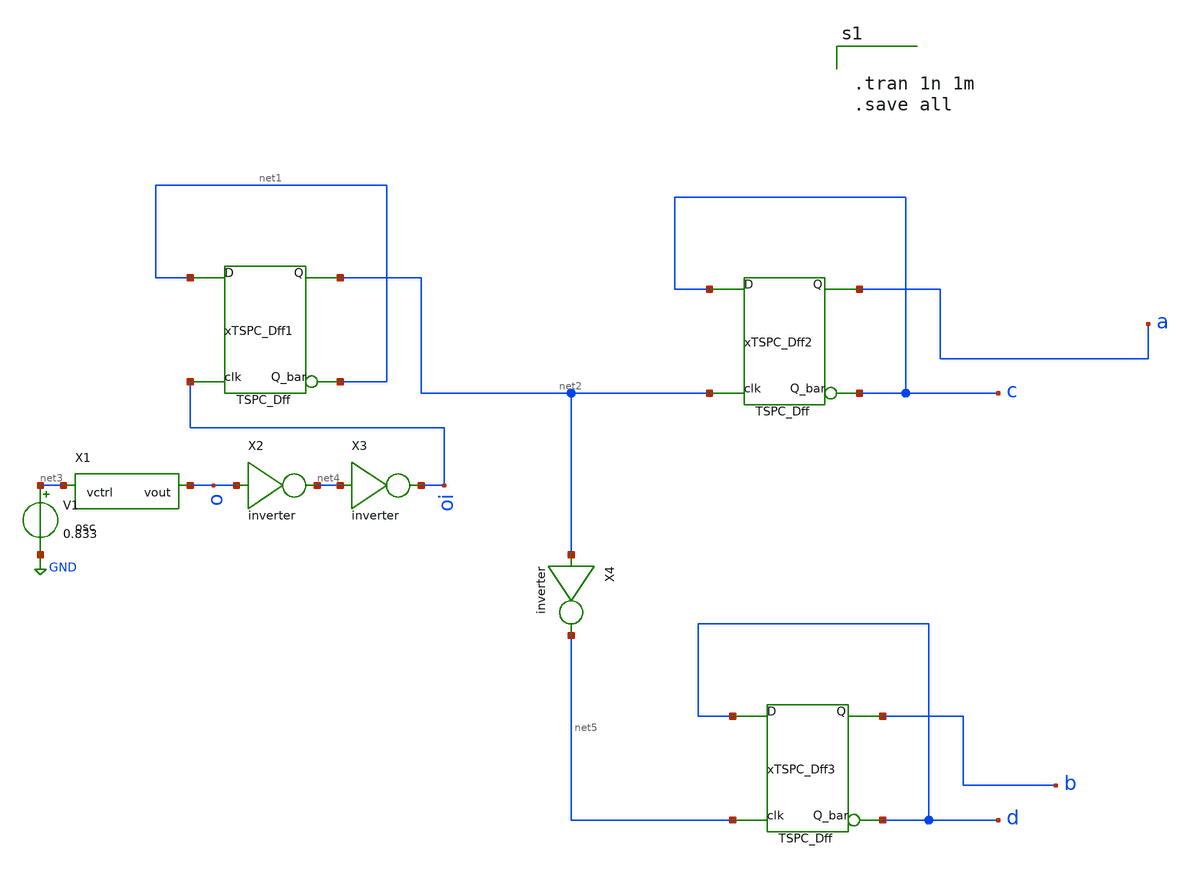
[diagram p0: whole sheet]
** sch_path: bfour.sch
**.subckt bfour
xTSPC_Dff1 oi net1 net1 net2 TSPC_Dff
X1 net3 o osc
V1 net3 GND 0.833
X2 o net4 inverter
X3 net4 oi inverter
xTSPC_Dff2 net2 c c a TSPC_Dff
xTSPC_Dff3 net5 d d b TSPC_Dff
X4 net2 net5 inverter
**** begin user architecture code


.tran 1n 1m
.save all


*.lib ~/open_pdks/sky130/sky130A/libs.tech/ngspice/sky130.lib.spice tt
.param mc_mm_switch=0
.param mc_pr_switch=0

.include ~/open_pdks/sky130/sky130A/libs.tech/ngspice/corners/tt/nonfet.spice


*model
.include ~/open_pdks/sky130/sky130A/libs.tech/ngspice/all.spice

*mosfet
.include ~/open_pdks/sky130/sky130A/libs.ref/sky130_fd_pr/spice/sky130_fd_pr__pfet_01v8__tt.corner.spice
.inclued ~/open_pdks/sky130/sky130A/libs.ref/sky130_fd_pr/spice/sky130_fd_pr__nfet_01v8__tt.corner.spice

*mismatch parameters
.include ~/open_pdks/sky130/sky130A/libs.ref/sky130_fd_pr/spice/sky130_fd_pr__pfet_01v8__mismatch.corner.spice
.include ~/open_pdks/sky130/sky130A/libs.ref/sky130_fd_pr/spice/sky130_fd_pr__nfet_01v8__mismatch.corner.spice

**** end user architecture code
**.ends

* expanding   symbol:  /home/cegrahul/Downloads/TSPC_Dff.sym # of pins=4
** sym_path: TSPC_Dff.sym
** sch_path: TSPC_Dff.sch
.subckt TSPC_Dff CLK D QB Q
*.ipin D
*.ipin CLK
*.opin Q
*.opin QB
V1 VDD GND 1.8
XM3 voutfirst D GND GND sky130_fd_pr__nfet_01v8 L=0.15 W=0.36 nf=1 ad='int((nf+1)/2) * W/nf * 0.29' as='int((nf+2)/2) * W/nf * 0.29'
+ pd='2*int((nf+1)/2) * (W/nf + 0.29)' ps='2*int((nf+2)/2) * (W/nf + 0.29)' nrd='0.29 / W' nrs='0.29 / W'
+ sa=0 sb=0 sd=0 mult=1 m=1
XM4 net1 D VDD VDD sky130_fd_pr__pfet_01v8 L=0.15 W=1.68 nf=1 ad='int((nf+1)/2) * W/nf * 0.29' as='int((nf+2)/2) * W/nf * 0.29'
+ pd='2*int((nf+1)/2) * (W/nf + 0.29)' ps='2*int((nf+2)/2) * (W/nf + 0.29)' nrd='0.29 / W' nrs='0.29 / W'
+ sa=0 sb=0 sd=0 mult=1 m=1
XM5 voutfirst CLK net1 VDD sky130_fd_pr__pfet_01v8 L=0.15 W=1.68 nf=1 ad='int((nf+1)/2) * W/nf * 0.29'
+ as='int((nf+2)/2) * W/nf * 0.29' pd='2*int((nf+1)/2) * (W/nf + 0.29)' ps='2*int((nf+2)/2) * (W/nf + 0.29)'
+ nrd='0.29 / W' nrs='0.29 / W' sa=0 sb=0 sd=0 mult=1 m=1
XM1 net3 CLK GND GND sky130_fd_pr__nfet_01v8 L=0.15 W=0.36 nf=1 ad='int((nf+1)/2) * W/nf * 0.29' as='int((nf+2)/2) * W/nf * 0.29'
+ pd='2*int((nf+1)/2) * (W/nf + 0.29)' ps='2*int((nf+2)/2) * (W/nf + 0.29)' nrd='0.29 / W' nrs='0.29 / W'
+ sa=0 sb=0 sd=0 mult=1 m=1
XM2 net2 CLK VDD VDD sky130_fd_pr__pfet_01v8 L=0.15 W=1.68 nf=1 ad='int((nf+1)/2) * W/nf * 0.29' as='int((nf+2)/2) * W/nf * 0.29'
+ pd='2*int((nf+1)/2) * (W/nf + 0.29)' ps='2*int((nf+2)/2) * (W/nf + 0.29)' nrd='0.29 / W' nrs='0.29 / W'
+ sa=0 sb=0 sd=0 mult=1 m=1
XM6 net2 voutfirst net3 GND sky130_fd_pr__nfet_01v8 L=0.15 W=0.36 nf=1 ad='int((nf+1)/2) * W/nf * 0.29'
+ as='int((nf+2)/2) * W/nf * 0.29' pd='2*int((nf+1)/2) * (W/nf + 0.29)' ps='2*int((nf+2)/2) * (W/nf + 0.29)'
+ nrd='0.29 / W' nrs='0.29 / W' sa=0 sb=0 sd=0 mult=1 m=1
XM7 net4 net2 GND GND sky130_fd_pr__nfet_01v8 L=2 W=0.42 nf=1 ad='int((nf+1)/2) * W/nf * 0.29' as='int((nf+2)/2) * W/nf * 0.29'
+ pd='2*int((nf+1)/2) * (W/nf + 0.29)' ps='2*int((nf+2)/2) * (W/nf + 0.29)' nrd='0.29 / W' nrs='0.29 / W'
+ sa=0 sb=0 sd=0 mult=1 m=1
XM8 voutthird net2 VDD VDD sky130_fd_pr__pfet_01v8 L=0.15 W=1.68 nf=1 ad='int((nf+1)/2) * W/nf * 0.29'
+ as='int((nf+2)/2) * W/nf * 0.29' pd='2*int((nf+1)/2) * (W/nf + 0.29)' ps='2*int((nf+2)/2) * (W/nf + 0.29)'
+ nrd='0.29 / W' nrs='0.29 / W' sa=0 sb=0 sd=0 mult=1 m=1
XM9 voutthird CLK net4 GND sky130_fd_pr__nfet_01v8 L=2 W=0.42 nf=1 ad='int((nf+1)/2) * W/nf * 0.29' as='int((nf+2)/2) * W/nf * 0.29'
+ pd='2*int((nf+1)/2) * (W/nf + 0.29)' ps='2*int((nf+2)/2) * (W/nf + 0.29)' nrd='0.29 / W' nrs='0.29 / W'
+ sa=0 sb=0 sd=0 mult=1 m=1
x1 voutthird Q inverter
x2 Q QB inverter
.ends


* expanding   symbol:  /home/cegrahul/Desktop/SSCS/osc.sym # of pins=2
** sym_path: osc.sym
** sch_path: osc.sch
.subckt osc vctrl vout
*.ipin vctrl
*.opin vout
XM1 net1 vout net2 GND sky130_fd_pr__nfet_01v8 L=4 W=0.55 nf=1 ad='int((nf+1)/2) * W/nf * 0.29' as='int((nf+2)/2) * W/nf * 0.29'
+ pd='2*int((nf+1)/2) * (W/nf + 0.29)' ps='2*int((nf+2)/2) * (W/nf + 0.29)' nrd='0.29 / W' nrs='0.29 / W'
+ sa=0 sb=0 sd=0 mult=1 m=1
XM3 net1 vout net3 net4 sky130_fd_pr__pfet_01v8 L=4 W=1 nf=1 ad='int((nf+1)/2) * W/nf * 0.29' as='int((nf+2)/2) * W/nf * 0.29'
+ pd='2*int((nf+1)/2) * (W/nf + 0.29)' ps='2*int((nf+2)/2) * (W/nf + 0.29)' nrd='0.29 / W' nrs='0.29 / W'
+ sa=0 sb=0 sd=0 mult=1 m=1
XM19 net2 vout GND GND sky130_fd_pr__nfet_01v8 L=4 W=0.55 nf=1 ad='int((nf+1)/2) * W/nf * 0.29' as='int((nf+2)/2) * W/nf * 0.29'
+ pd='2*int((nf+1)/2) * (W/nf + 0.29)' ps='2*int((nf+2)/2) * (W/nf + 0.29)' nrd='0.29 / W' nrs='0.29 / W'
+ sa=0 sb=0 sd=0 mult=1 m=1
XM29 net3 vctrl net4 net4 sky130_fd_pr__pfet_01v8 L=2 W=1 nf=1 ad='int((nf+1)/2) * W/nf * 0.29' as='int((nf+2)/2) * W/nf * 0.29'
+ pd='2*int((nf+1)/2) * (W/nf + 0.29)' ps='2*int((nf+2)/2) * (W/nf + 0.29)' nrd='0.29 / W' nrs='0.29 / W'
+ sa=0 sb=0 sd=0 mult=1 m=1
V3 net4 GND 1.8
XM2 net5 net1 net6 GND sky130_fd_pr__nfet_01v8 L=4 W=0.55 nf=1 ad='int((nf+1)/2) * W/nf * 0.29' as='int((nf+2)/2) * W/nf * 0.29'
+ pd='2*int((nf+1)/2) * (W/nf + 0.29)' ps='2*int((nf+2)/2) * (W/nf + 0.29)' nrd='0.29 / W' nrs='0.29 / W'
+ sa=0 sb=0 sd=0 mult=1 m=1
XM4 net5 net1 net3 net4 sky130_fd_pr__pfet_01v8 L=4 W=1 nf=1 ad='int((nf+1)/2) * W/nf * 0.29' as='int((nf+2)/2) * W/nf * 0.29'
+ pd='2*int((nf+1)/2) * (W/nf + 0.29)' ps='2*int((nf+2)/2) * (W/nf + 0.29)' nrd='0.29 / W' nrs='0.29 / W'
+ sa=0 sb=0 sd=0 mult=1 m=1
XM5 net6 net1 GND GND sky130_fd_pr__nfet_01v8 L=4 W=0.55 nf=1 ad='int((nf+1)/2) * W/nf * 0.29' as='int((nf+2)/2) * W/nf * 0.29'
+ pd='2*int((nf+1)/2) * (W/nf + 0.29)' ps='2*int((nf+2)/2) * (W/nf + 0.29)' nrd='0.29 / W' nrs='0.29 / W'
+ sa=0 sb=0 sd=0 mult=1 m=1
XM6 net3 vctrl net4 net4 sky130_fd_pr__pfet_01v8 L=2 W=1 nf=1 ad='int((nf+1)/2) * W/nf * 0.29' as='int((nf+2)/2) * W/nf * 0.29'
+ pd='2*int((nf+1)/2) * (W/nf + 0.29)' ps='2*int((nf+2)/2) * (W/nf + 0.29)' nrd='0.29 / W' nrs='0.29 / W'
+ sa=0 sb=0 sd=0 mult=1 m=1
XM7 net7 net5 net8 GND sky130_fd_pr__nfet_01v8 L=4 W=0.55 nf=1 ad='int((nf+1)/2) * W/nf * 0.29' as='int((nf+2)/2) * W/nf * 0.29'
+ pd='2*int((nf+1)/2) * (W/nf + 0.29)' ps='2*int((nf+2)/2) * (W/nf + 0.29)' nrd='0.29 / W' nrs='0.29 / W'
+ sa=0 sb=0 sd=0 mult=1 m=1
XM8 net7 net5 net3 net4 sky130_fd_pr__pfet_01v8 L=4 W=1 nf=1 ad='int((nf+1)/2) * W/nf * 0.29' as='int((nf+2)/2) * W/nf * 0.29'
+ pd='2*int((nf+1)/2) * (W/nf + 0.29)' ps='2*int((nf+2)/2) * (W/nf + 0.29)' nrd='0.29 / W' nrs='0.29 / W'
+ sa=0 sb=0 sd=0 mult=1 m=1
XM9 net8 net5 GND GND sky130_fd_pr__nfet_01v8 L=4 W=0.55 nf=1 ad='int((nf+1)/2) * W/nf * 0.29' as='int((nf+2)/2) * W/nf * 0.29'
+ pd='2*int((nf+1)/2) * (W/nf + 0.29)' ps='2*int((nf+2)/2) * (W/nf + 0.29)' nrd='0.29 / W' nrs='0.29 / W'
+ sa=0 sb=0 sd=0 mult=1 m=1
XM10 net3 vctrl net4 net4 sky130_fd_pr__pfet_01v8 L=2 W=1 nf=1 ad='int((nf+1)/2) * W/nf * 0.29' as='int((nf+2)/2) * W/nf * 0.29'
+ pd='2*int((nf+1)/2) * (W/nf + 0.29)' ps='2*int((nf+2)/2) * (W/nf + 0.29)' nrd='0.29 / W' nrs='0.29 / W'
+ sa=0 sb=0 sd=0 mult=1 m=1
XM11 net9 net7 net10 GND sky130_fd_pr__nfet_01v8 L=4 W=0.55 nf=1 ad='int((nf+1)/2) * W/nf * 0.29' as='int((nf+2)/2) * W/nf * 0.29'
+ pd='2*int((nf+1)/2) * (W/nf + 0.29)' ps='2*int((nf+2)/2) * (W/nf + 0.29)' nrd='0.29 / W' nrs='0.29 / W'
+ sa=0 sb=0 sd=0 mult=1 m=1
XM12 net9 net7 net3 net4 sky130_fd_pr__pfet_01v8 L=4 W=1 nf=1 ad='int((nf+1)/2) * W/nf * 0.29' as='int((nf+2)/2) * W/nf * 0.29'
+ pd='2*int((nf+1)/2) * (W/nf + 0.29)' ps='2*int((nf+2)/2) * (W/nf + 0.29)' nrd='0.29 / W' nrs='0.29 / W'
+ sa=0 sb=0 sd=0 mult=1 m=1
XM13 net10 net7 GND GND sky130_fd_pr__nfet_01v8 L=4 W=0.55 nf=1 ad='int((nf+1)/2) * W/nf * 0.29' as='int((nf+2)/2) * W/nf * 0.29'
+ pd='2*int((nf+1)/2) * (W/nf + 0.29)' ps='2*int((nf+2)/2) * (W/nf + 0.29)' nrd='0.29 / W' nrs='0.29 / W'
+ sa=0 sb=0 sd=0 mult=1 m=1
XM14 net3 vctrl net4 net4 sky130_fd_pr__pfet_01v8 L=2 W=1 nf=1 ad='int((nf+1)/2) * W/nf * 0.29' as='int((nf+2)/2) * W/nf * 0.29'
+ pd='2*int((nf+1)/2) * (W/nf + 0.29)' ps='2*int((nf+2)/2) * (W/nf + 0.29)' nrd='0.29 / W' nrs='0.29 / W'
+ sa=0 sb=0 sd=0 mult=1 m=1
XM15 net11 net9 net12 GND sky130_fd_pr__nfet_01v8 L=4 W=0.55 nf=1 ad='int((nf+1)/2) * W/nf * 0.29' as='int((nf+2)/2) * W/nf * 0.29'
+ pd='2*int((nf+1)/2) * (W/nf + 0.29)' ps='2*int((nf+2)/2) * (W/nf + 0.29)' nrd='0.29 / W' nrs='0.29 / W'
+ sa=0 sb=0 sd=0 mult=1 m=1
XM16 net11 net9 net3 net4 sky130_fd_pr__pfet_01v8 L=4 W=1 nf=1 ad='int((nf+1)/2) * W/nf * 0.29' as='int((nf+2)/2) * W/nf * 0.29'
+ pd='2*int((nf+1)/2) * (W/nf + 0.29)' ps='2*int((nf+2)/2) * (W/nf + 0.29)' nrd='0.29 / W' nrs='0.29 / W'
+ sa=0 sb=0 sd=0 mult=1 m=1
XM17 net12 net9 GND GND sky130_fd_pr__nfet_01v8 L=4 W=0.55 nf=1 ad='int((nf+1)/2) * W/nf * 0.29' as='int((nf+2)/2) * W/nf * 0.29'
+ pd='2*int((nf+1)/2) * (W/nf + 0.29)' ps='2*int((nf+2)/2) * (W/nf + 0.29)' nrd='0.29 / W' nrs='0.29 / W'
+ sa=0 sb=0 sd=0 mult=1 m=1
XM18 net3 vctrl net4 net4 sky130_fd_pr__pfet_01v8 L=2 W=1 nf=1 ad='int((nf+1)/2) * W/nf * 0.29' as='int((nf+2)/2) * W/nf * 0.29'
+ pd='2*int((nf+1)/2) * (W/nf + 0.29)' ps='2*int((nf+2)/2) * (W/nf + 0.29)' nrd='0.29 / W' nrs='0.29 / W'
+ sa=0 sb=0 sd=0 mult=1 m=1
XM20 net13 net11 net14 GND sky130_fd_pr__nfet_01v8 L=4 W=0.55 nf=1 ad='int((nf+1)/2) * W/nf * 0.29' as='int((nf+2)/2) * W/nf * 0.29'
+ pd='2*int((nf+1)/2) * (W/nf + 0.29)' ps='2*int((nf+2)/2) * (W/nf + 0.29)' nrd='0.29 / W' nrs='0.29 / W'
+ sa=0 sb=0 sd=0 mult=1 m=1
XM21 net13 net11 net3 net4 sky130_fd_pr__pfet_01v8 L=4 W=1 nf=1 ad='int((nf+1)/2) * W/nf * 0.29' as='int((nf+2)/2) * W/nf * 0.29'
+ pd='2*int((nf+1)/2) * (W/nf + 0.29)' ps='2*int((nf+2)/2) * (W/nf + 0.29)' nrd='0.29 / W' nrs='0.29 / W'
+ sa=0 sb=0 sd=0 mult=1 m=1
XM22 net14 net11 GND GND sky130_fd_pr__nfet_01v8 L=4 W=0.55 nf=1 ad='int((nf+1)/2) * W/nf * 0.29' as='int((nf+2)/2) * W/nf * 0.29'
+ pd='2*int((nf+1)/2) * (W/nf + 0.29)' ps='2*int((nf+2)/2) * (W/nf + 0.29)' nrd='0.29 / W' nrs='0.29 / W'
+ sa=0 sb=0 sd=0 mult=1 m=1
XM23 net3 vctrl net4 net4 sky130_fd_pr__pfet_01v8 L=2 W=1 nf=1 ad='int((nf+1)/2) * W/nf * 0.29' as='int((nf+2)/2) * W/nf * 0.29'
+ pd='2*int((nf+1)/2) * (W/nf + 0.29)' ps='2*int((nf+2)/2) * (W/nf + 0.29)' nrd='0.29 / W' nrs='0.29 / W'
+ sa=0 sb=0 sd=0 mult=1 m=1
XM24 net15 net13 net16 GND sky130_fd_pr__nfet_01v8 L=4 W=0.55 nf=1 ad='int((nf+1)/2) * W/nf * 0.29' as='int((nf+2)/2) * W/nf * 0.29'
+ pd='2*int((nf+1)/2) * (W/nf + 0.29)' ps='2*int((nf+2)/2) * (W/nf + 0.29)' nrd='0.29 / W' nrs='0.29 / W'
+ sa=0 sb=0 sd=0 mult=1 m=1
XM25 net15 net13 net3 net4 sky130_fd_pr__pfet_01v8 L=4 W=1 nf=1 ad='int((nf+1)/2) * W/nf * 0.29' as='int((nf+2)/2) * W/nf * 0.29'
+ pd='2*int((nf+1)/2) * (W/nf + 0.29)' ps='2*int((nf+2)/2) * (W/nf + 0.29)' nrd='0.29 / W' nrs='0.29 / W'
+ sa=0 sb=0 sd=0 mult=1 m=1
XM26 net16 net13 GND GND sky130_fd_pr__nfet_01v8 L=4 W=0.55 nf=1 ad='int((nf+1)/2) * W/nf * 0.29' as='int((nf+2)/2) * W/nf * 0.29'
+ pd='2*int((nf+1)/2) * (W/nf + 0.29)' ps='2*int((nf+2)/2) * (W/nf + 0.29)' nrd='0.29 / W' nrs='0.29 / W'
+ sa=0 sb=0 sd=0 mult=1 m=1
XM27 net3 vctrl net4 net4 sky130_fd_pr__pfet_01v8 L=2 W=1 nf=1 ad='int((nf+1)/2) * W/nf * 0.29' as='int((nf+2)/2) * W/nf * 0.29'
+ pd='2*int((nf+1)/2) * (W/nf + 0.29)' ps='2*int((nf+2)/2) * (W/nf + 0.29)' nrd='0.29 / W' nrs='0.29 / W'
+ sa=0 sb=0 sd=0 mult=1 m=1
XM28 net17 net15 net18 GND sky130_fd_pr__nfet_01v8 L=4 W=0.55 nf=1 ad='int((nf+1)/2) * W/nf * 0.29' as='int((nf+2)/2) * W/nf * 0.29'
+ pd='2*int((nf+1)/2) * (W/nf + 0.29)' ps='2*int((nf+2)/2) * (W/nf + 0.29)' nrd='0.29 / W' nrs='0.29 / W'
+ sa=0 sb=0 sd=0 mult=1 m=1
XM30 net17 net15 net3 net4 sky130_fd_pr__pfet_01v8 L=4 W=1 nf=1 ad='int((nf+1)/2) * W/nf * 0.29' as='int((nf+2)/2) * W/nf * 0.29'
+ pd='2*int((nf+1)/2) * (W/nf + 0.29)' ps='2*int((nf+2)/2) * (W/nf + 0.29)' nrd='0.29 / W' nrs='0.29 / W'
+ sa=0 sb=0 sd=0 mult=1 m=1
XM31 net18 net15 GND GND sky130_fd_pr__nfet_01v8 L=4 W=0.55 nf=1 ad='int((nf+1)/2) * W/nf * 0.29' as='int((nf+2)/2) * W/nf * 0.29'
+ pd='2*int((nf+1)/2) * (W/nf + 0.29)' ps='2*int((nf+2)/2) * (W/nf + 0.29)' nrd='0.29 / W' nrs='0.29 / W'
+ sa=0 sb=0 sd=0 mult=1 m=1
XM32 net3 vctrl net4 net4 sky130_fd_pr__pfet_01v8 L=2 W=1 nf=1 ad='int((nf+1)/2) * W/nf * 0.29' as='int((nf+2)/2) * W/nf * 0.29'
+ pd='2*int((nf+1)/2) * (W/nf + 0.29)' ps='2*int((nf+2)/2) * (W/nf + 0.29)' nrd='0.29 / W' nrs='0.29 / W'
+ sa=0 sb=0 sd=0 mult=1 m=1
XM33 vout net17 net19 GND sky130_fd_pr__nfet_01v8 L=4 W=0.55 nf=1 ad='int((nf+1)/2) * W/nf * 0.29' as='int((nf+2)/2) * W/nf * 0.29'
+ pd='2*int((nf+1)/2) * (W/nf + 0.29)' ps='2*int((nf+2)/2) * (W/nf + 0.29)' nrd='0.29 / W' nrs='0.29 / W'
+ sa=0 sb=0 sd=0 mult=1 m=1
XM34 vout net17 net3 net4 sky130_fd_pr__pfet_01v8 L=4 W=1 nf=1 ad='int((nf+1)/2) * W/nf * 0.29' as='int((nf+2)/2) * W/nf * 0.29'
+ pd='2*int((nf+1)/2) * (W/nf + 0.29)' ps='2*int((nf+2)/2) * (W/nf + 0.29)' nrd='0.29 / W' nrs='0.29 / W'
+ sa=0 sb=0 sd=0 mult=1 m=1
XM35 net19 net17 GND GND sky130_fd_pr__nfet_01v8 L=4 W=0.55 nf=1 ad='int((nf+1)/2) * W/nf * 0.29' as='int((nf+2)/2) * W/nf * 0.29'
+ pd='2*int((nf+1)/2) * (W/nf + 0.29)' ps='2*int((nf+2)/2) * (W/nf + 0.29)' nrd='0.29 / W' nrs='0.29 / W'
+ sa=0 sb=0 sd=0 mult=1 m=1
XM36 net3 vctrl net4 net4 sky130_fd_pr__pfet_01v8 L=2 W=1 nf=1 ad='int((nf+1)/2) * W/nf * 0.29' as='int((nf+2)/2) * W/nf * 0.29'
+ pd='2*int((nf+1)/2) * (W/nf + 0.29)' ps='2*int((nf+2)/2) * (W/nf + 0.29)' nrd='0.29 / W' nrs='0.29 / W'
+ sa=0 sb=0 sd=0 mult=1 m=1
.ends


* expanding   symbol:  /home/cegrahul/Desktop/SSCS/inverter.sym # of pins=2
** sym_path: inverter.sym
** sch_path: inverter.sch
.subckt inverter vin vout
*.ipin vin
*.opin vout
XM2 vout vin net1 net1 sky130_fd_pr__pfet_01v8 L=0.15 W=1.68 nf=1 ad='int((nf+1)/2) * W/nf * 0.29' as='int((nf+2)/2) * W/nf * 0.29'
+ pd='2*int((nf+1)/2) * (W/nf + 0.29)' ps='2*int((nf+2)/2) * (W/nf + 0.29)' nrd='0.29 / W' nrs='0.29 / W'
+ sa=0 sb=0 sd=0 mult=1 m=1
XM3 vout vin GND GND sky130_fd_pr__nfet_01v8 L=0.15 W=0.36 nf=1 ad='int((nf+1)/2) * W/nf * 0.29' as='int((nf+2)/2) * W/nf * 0.29'
+ pd='2*int((nf+1)/2) * (W/nf + 0.29)' ps='2*int((nf+2)/2) * (W/nf + 0.29)' nrd='0.29 / W' nrs='0.29 / W'
+ sa=0 sb=0 sd=0 mult=1 m=1
V3 net1 GND 1.8
.ends

.GLOBAL GND
.end
